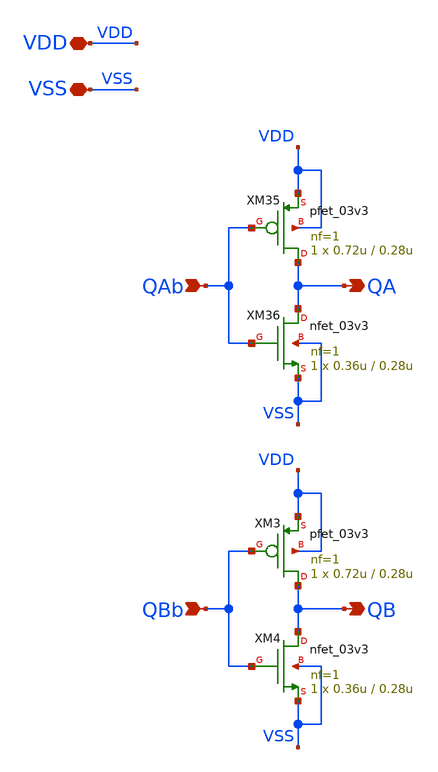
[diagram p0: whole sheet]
** sch_path: CAD3/output_inverter.sch
**.subckt output_inverter QB QA VDD VSS QAb QBb
*.opin QB
*.opin QA
*.iopin VDD
*.iopin VSS
*.ipin QAb
*.ipin QBb
XM3 QB QBb VDD VDD pfet_03v3 L=0.28u W=0.72u nf=1 ad='int((nf+1)/2) * W/nf * 0.18u' as='int((nf+2)/2) * W/nf * 0.18u'
+ pd='2*int((nf+1)/2) * (W/nf + 0.18u)' ps='2*int((nf+2)/2) * (W/nf + 0.18u)' nrd='0.18u / W' nrs='0.18u / W'
+ sa=0 sb=0 sd=0 m=1
XM4 QB QBb VSS VSS nfet_03v3 L=0.28u W=0.36u nf=1 ad='int((nf+1)/2) * W/nf * 0.18u' as='int((nf+2)/2) * W/nf * 0.18u'
+ pd='2*int((nf+1)/2) * (W/nf + 0.18u)' ps='2*int((nf+2)/2) * (W/nf + 0.18u)' nrd='0.18u / W' nrs='0.18u / W'
+ sa=0 sb=0 sd=0 m=1
XM35 QA QAb VDD VDD pfet_03v3 L=0.28u W=0.72u nf=1 ad='int((nf+1)/2) * W/nf * 0.18u' as='int((nf+2)/2) * W/nf * 0.18u'
+ pd='2*int((nf+1)/2) * (W/nf + 0.18u)' ps='2*int((nf+2)/2) * (W/nf + 0.18u)' nrd='0.18u / W' nrs='0.18u / W'
+ sa=0 sb=0 sd=0 m=1
XM36 QA QAb VSS VSS nfet_03v3 L=0.28u W=0.36u nf=1 ad='int((nf+1)/2) * W/nf * 0.18u' as='int((nf+2)/2) * W/nf * 0.18u'
+ pd='2*int((nf+1)/2) * (W/nf + 0.18u)' ps='2*int((nf+2)/2) * (W/nf + 0.18u)' nrd='0.18u / W' nrs='0.18u / W'
+ sa=0 sb=0 sd=0 m=1
**.ends
.end
